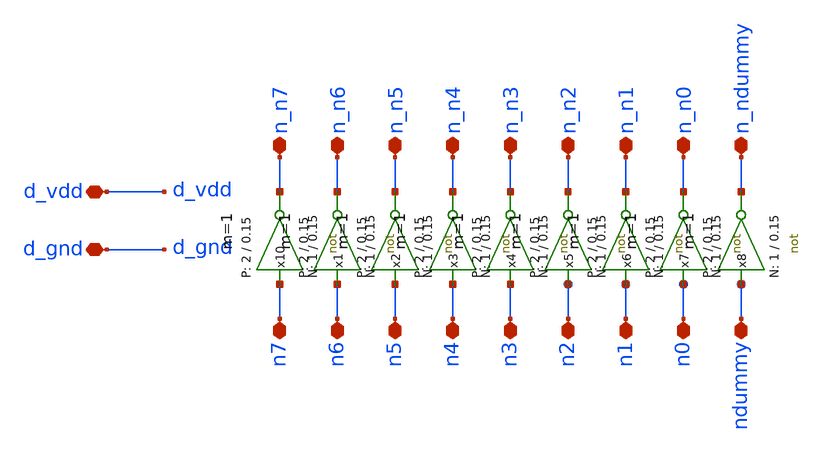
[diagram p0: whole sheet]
** sch_path: Schematics/ADC/inverter_array/inverter_array.sch
* StefanSchippers/xschem_sky130/sky130_tests/not.sch:
* Copyright 2021 Stefan Frederik Schippers
* Licensed under the Apache License, Version 2.0 (the "License");
**.subckt inverter_array n_n7 n_n6 n7 n6 n5 n4 n3 n2 n1 n0 ndummy n_n5 n_n4 n_n3 n_n2 n_n1 n_n0
*+ n_ndummy d_gnd d_vdd
*.iopin n_n7
*.iopin n_n6
*.iopin n7
*.iopin n6
*.iopin n5
*.iopin n4
*.iopin n3
*.iopin n2
*.iopin n1
*.iopin n0
*.iopin ndummy
*.iopin n_n5
*.iopin n_n4
*.iopin n_n3
*.iopin n_n2
*.iopin n_n1
*.iopin n_n0
*.iopin n_ndummy
*.iopin d_gnd
*.iopin d_vdd
x10 n_n7 n7 d_vdd d_gnd not W_N=1 L_N=0.15 W_P=2 L_P=0.15 m=1
x1 n_n6 n6 d_vdd d_gnd not W_N=1 L_N=0.15 W_P=2 L_P=0.15 m=1
x2 n_n5 n5 d_vdd d_gnd not W_N=1 L_N=0.15 W_P=2 L_P=0.15 m=1
x3 n_n4 n4 d_vdd d_gnd not W_N=1 L_N=0.15 W_P=2 L_P=0.15 m=1
x4 n_n3 n3 d_vdd d_gnd not W_N=1 L_N=0.15 W_P=2 L_P=0.15 m=1
x5 n_n2 n2 d_vdd d_gnd not W_N=1 L_N=0.15 W_P=2 L_P=0.15 m=1
x6 n_n1 n1 d_vdd d_gnd not W_N=1 L_N=0.15 W_P=2 L_P=0.15 m=1
x7 n_n0 n0 d_vdd d_gnd not W_N=1 L_N=0.15 W_P=2 L_P=0.15 m=1
x8 n_ndummy ndummy d_vdd d_gnd not W_N=1 L_N=0.15 W_P=2 L_P=0.15 m=1
**.ends

* expanding   symbol:  /home/richmond/pdk/sky130A/libs.tech/xschem/sky130_tests/not.sym # of pins=2
** sym_path: /home/richmond/pdk/sky130A/libs.tech/xschem/sky130_tests/not.sym
** sch_path: /home/richmond/pdk/sky130A/libs.tech/xschem/sky130_tests/not.sch
.subckt not y a VCCPIN VSSPIN     W_N=1 L_N=0.15 W_P=2 L_P=0.15
*.opin y
*.ipin a
XM1 DN a VSSPIN VSSPIN sky130_fd_pr__nfet_01v8 L=L_N W=W_N nf=1 ad='int((1 + 1)/2) * W_N / 1 * 0.29'
+ as='int((1 + 2)/2) * W_N / 1 * 0.29' pd='2*int((1 + 1)/2) * (W_N / 1 + 0.29)' ps='2*int((1 + 2)/2) * (W_N / 1 + 0.29)'
+ nrd='0.29 / W_N ' nrs='0.29 / W_N ' sa=0 sb=0 sd=0 mult=1 m=1
XM2 DP a VCCPIN VCCPIN sky130_fd_pr__pfet_01v8 L=L_P W=W_P nf=1 ad='int((nf+1)/2) * W/nf * 0.29' as='int((nf+2)/2) * W/nf * 0.29'
+ pd='2*int((nf+1)/2) * (W/nf + 0.29)' ps='2*int((nf+2)/2) * (W/nf + 0.29)' nrd='0.29 / W' nrs='0.29 / W'
+ sa=0 sb=0 sd=0 mult=1 m=1
Vmeas DP y 0
.save i(vmeas)
Vmeas1 y DN 0
.save i(vmeas1)
.save v(dp)
.save v(dn)
.ends

.end
